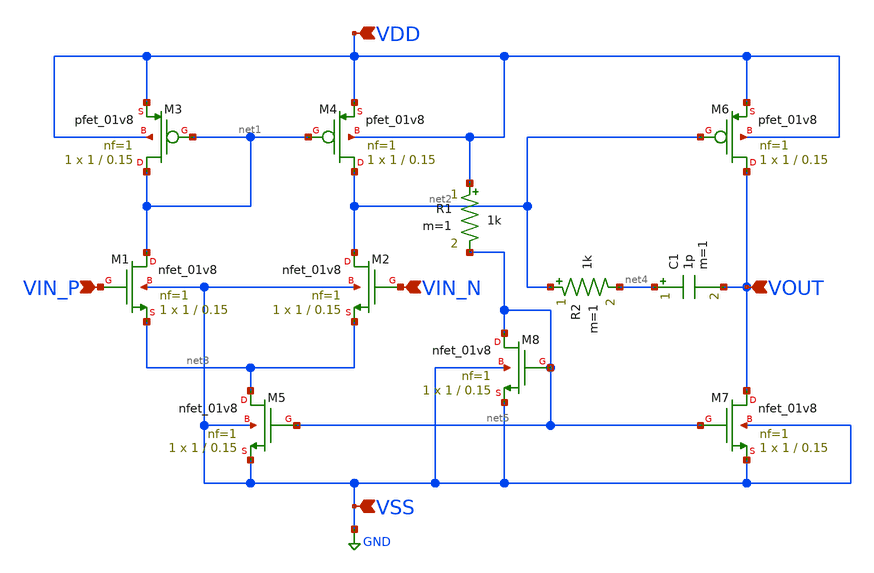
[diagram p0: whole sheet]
** sch_path: analog/schematics/bootcamp_opamp.sch
**.subckt bootcamp_opamp VIN_P VIN_N VDD VOUT VSS
*.ipin VIN_P
*.ipin VIN_N
*.ipin VDD
*.ipin VOUT
*.ipin VSS
XM1 net1 VIN_P net3 VSS sky130_fd_pr__nfet_01v8 L=0.15 W=1 nf=1 ad='int((nf+1)/2) * W/nf * 0.29' as='int((nf+2)/2) * W/nf * 0.29'
+ pd='2*int((nf+1)/2) * (W/nf + 0.29)' ps='2*int((nf+2)/2) * (W/nf + 0.29)' nrd='0.29 / W' nrs='0.29 / W'
+ sa=0 sb=0 sd=0 mult=1 m=1
XM2 net2 VIN_N net3 VSS sky130_fd_pr__nfet_01v8 L=0.15 W=1 nf=1 ad='int((nf+1)/2) * W/nf * 0.29' as='int((nf+2)/2) * W/nf * 0.29'
+ pd='2*int((nf+1)/2) * (W/nf + 0.29)' ps='2*int((nf+2)/2) * (W/nf + 0.29)' nrd='0.29 / W' nrs='0.29 / W'
+ sa=0 sb=0 sd=0 mult=1 m=1
XM3 net1 net1 VDD VDD sky130_fd_pr__pfet_01v8 L=0.15 W=1 nf=1 ad='int((nf+1)/2) * W/nf * 0.29' as='int((nf+2)/2) * W/nf * 0.29'
+ pd='2*int((nf+1)/2) * (W/nf + 0.29)' ps='2*int((nf+2)/2) * (W/nf + 0.29)' nrd='0.29 / W' nrs='0.29 / W'
+ sa=0 sb=0 sd=0 mult=1 m=1
XM4 net2 net1 VDD VDD sky130_fd_pr__pfet_01v8 L=0.15 W=1 nf=1 ad='int((nf+1)/2) * W/nf * 0.29' as='int((nf+2)/2) * W/nf * 0.29'
+ pd='2*int((nf+1)/2) * (W/nf + 0.29)' ps='2*int((nf+2)/2) * (W/nf + 0.29)' nrd='0.29 / W' nrs='0.29 / W'
+ sa=0 sb=0 sd=0 mult=1 m=1
XM5 net3 net5 VSS VSS sky130_fd_pr__nfet_01v8 L=0.15 W=1 nf=1 ad='int((nf+1)/2) * W/nf * 0.29' as='int((nf+2)/2) * W/nf * 0.29'
+ pd='2*int((nf+1)/2) * (W/nf + 0.29)' ps='2*int((nf+2)/2) * (W/nf + 0.29)' nrd='0.29 / W' nrs='0.29 / W'
+ sa=0 sb=0 sd=0 mult=1 m=1
XM6 VOUT net2 VDD VDD sky130_fd_pr__pfet_01v8 L=0.15 W=1 nf=1 ad='int((nf+1)/2) * W/nf * 0.29' as='int((nf+2)/2) * W/nf * 0.29'
+ pd='2*int((nf+1)/2) * (W/nf + 0.29)' ps='2*int((nf+2)/2) * (W/nf + 0.29)' nrd='0.29 / W' nrs='0.29 / W'
+ sa=0 sb=0 sd=0 mult=1 m=1
XM7 VOUT net5 VSS VSS sky130_fd_pr__nfet_01v8 L=0.15 W=1 nf=1 ad='int((nf+1)/2) * W/nf * 0.29' as='int((nf+2)/2) * W/nf * 0.29'
+ pd='2*int((nf+1)/2) * (W/nf + 0.29)' ps='2*int((nf+2)/2) * (W/nf + 0.29)' nrd='0.29 / W' nrs='0.29 / W'
+ sa=0 sb=0 sd=0 mult=1 m=1
R2 net2 net4 1k m=1
C1 net4 VOUT 1p m=1
XM8 net5 net5 VSS VSS sky130_fd_pr__nfet_01v8 L=0.15 W=1 nf=1 ad='int((nf+1)/2) * W/nf * 0.29' as='int((nf+2)/2) * W/nf * 0.29'
+ pd='2*int((nf+1)/2) * (W/nf + 0.29)' ps='2*int((nf+2)/2) * (W/nf + 0.29)' nrd='0.29 / W' nrs='0.29 / W'
+ sa=0 sb=0 sd=0 mult=1 m=1
R1 VDD net5 1k m=1
**.ends
.GLOBAL GND
.end
